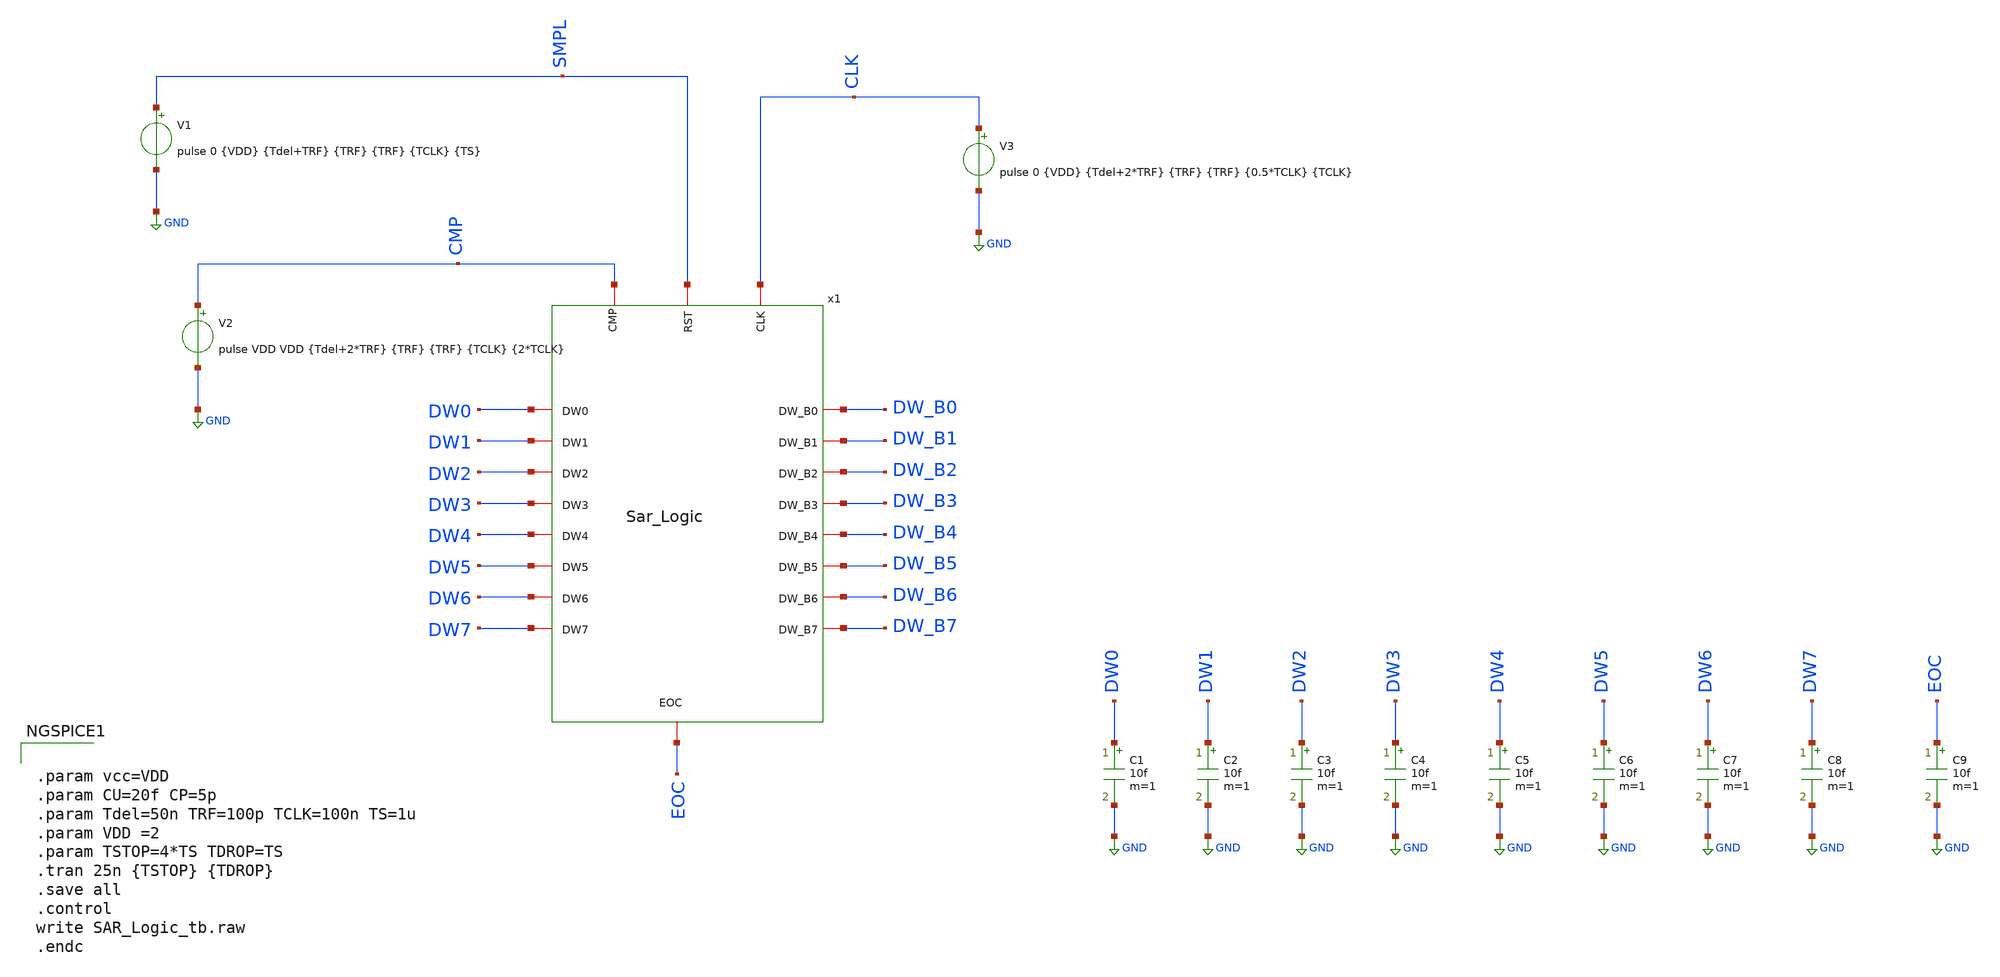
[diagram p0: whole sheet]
** sch_path: Designs/SAR_Logic_tb.sch
**.subckt SAR_Logic_tb
x1 CMP CLK EOC SMPL DW0 DW_B0 DW1 DW_B1 DW_B2 DW2 DW3 DW_B3 DW4 DW_B4 DW5 DW_B5 DW6 DW_B6 DW7 DW_B7
+ SAR_Logic
V1 SMPL GND pulse 0 {VDD} {Tdel+TRF} {TRF} {TRF} {TCLK} {TS}
V2 CMP GND pulse VDD VDD {Tdel+2*TRF} {TRF} {TRF} {TCLK} {2*TCLK}
V3 CLK GND pulse 0 {VDD} {Tdel+2*TRF} {TRF} {TRF} {0.5*TCLK} {TCLK}
C1 DW0 GND 10f m=1
C2 DW1 GND 10f m=1
C3 DW2 GND 10f m=1
C4 DW3 GND 10f m=1
C5 DW4 GND 10f m=1
C6 DW5 GND 10f m=1
C7 DW6 GND 10f m=1
C8 DW7 GND 10f m=1
C9 EOC GND 10f m=1
**** begin user architecture code


.param vcc=VDD
.param CU=20f CP=5p
.param Tdel=50n TRF=100p TCLK=100n TS=1u
.param VDD =2
.param TSTOP=4*TS TDROP=TS
.tran 25n {TSTOP} {TDROP}
.save all
.control
write SAR_Logic_tb.raw
.endc


**** end user architecture code
**.ends

* expanding   symbol:  /home/tare/Desktop/Analog design/SAR_Logic.sym # of pins=20
** sym_path: Designs/SAR_Logic.sym
** sch_path: Designs/SAR_Logic.sch
.subckt SAR_Logic CMP CLK EOC RST DW0 DW_B0 DW1 DW_B1 DW_B2 DW2 DW3 DW_B3 DW4 DW_B4 DW5 DW_B5 DW6
+ DW_B6 DW7 DW_B7
*.iopin DW0
*.iopin DW1
*.iopin DW2
*.iopin DW3
*.iopin DW4
*.iopin DW5
*.iopin DW6
*.iopin DW7
*.iopin DW_B0
*.iopin DW_B1
*.iopin DW_B2
*.iopin DW_B3
*.iopin DW_B4
*.iopin DW_B5
*.iopin DW_B6
*.iopin DW_B7
*.iopin CMP
*.iopin CLK
*.iopin RST
*.iopin EOC
**** begin user architecture code


a1 0 CLK RST 0 QCNT8 QCNT_B8 flop1
a2 QCNT8 CLK 0 RST QCNT7 QCNT_B7 flop1
a3 QCNT7 CLK 0 RST QCNT6 QCNT_B6 flop1
a4 QCNT6 CLK 0 RST QCNT5 QCNT_B5 flop1
a5 QCNT5 CLK 0 RST QCNT4 QCNT_B4 flop1
a6 QCNT4 CLK 0 RST QCNT3 QCNT_B3 flop1
a7 QCNT3 CLK 0 RST QCNT2 QCNT_B2 flop1
a8 QCNT2 CLK 0 RST QCNT1 QCNT_B1 flop1
a9 QCNT1 CLK 0 RST QCNT0 QCNT_B0 flop1
a10 CMP DW6 QCNT8 0 DW7 DW_B7 flop1
a11 CMP DW5 QCNT7 RST DW6 DW_B6 flop1
a12 CMP DW4 QCNT6 RST DW5 DW_B5 flop1
a13 CMP DW3 QCNT5 RST DW4 DW_B4 flop1
a14 CMP DW2 QCNT4 RST DW3 DW_B3 flop1
a15 CMP DW1 QCNT3 RST DW2 DW_B2 flop1
a16 CMP DW0 QCNT2 RST DW1 DW_B1 flop1
a17 CMP EOC QCNT1 RST DW0 DW_B0 flop1
a18 0 0 QCNT0 RST EOC NOOP flop1
.model flop1 d_dff(clk_delay = 10e-9 set_delay = 100e-12  reset_delay = 100e-12 ic =1.8 rise_delay =
+ 100e-12  fall_delay = 100e-12)


**** end user architecture code
.ends

.GLOBAL GND
.end
